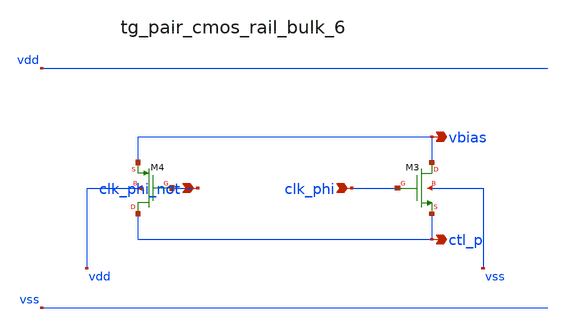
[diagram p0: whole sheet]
** sch_path: analog-db/raw/cmfb_004_output_switched_cap/hier/blocks/tg_pair_cmos_rail_bulk_6.sch
**.subckt tg_pair_cmos_rail_bulk_6 clk_phi_not clk_phi vbias ctl_p
*.ipin clk_phi_not
*.ipin clk_phi
*.opin vbias
*.opin ctl_p
XM3 vbias clk_phi ctl_p vss sg13_lv_nmos w=x_dut_xm3_w l=x_dut_xm3_l ng=1 m=x_dut_xm3_m
XM4 ctl_p clk_phi_not vbias vdd sg13_lv_pmos w=x_dut_xm4_w l=x_dut_xm4_l ng=1 m=x_dut_xm4_m
**.ends
.end
